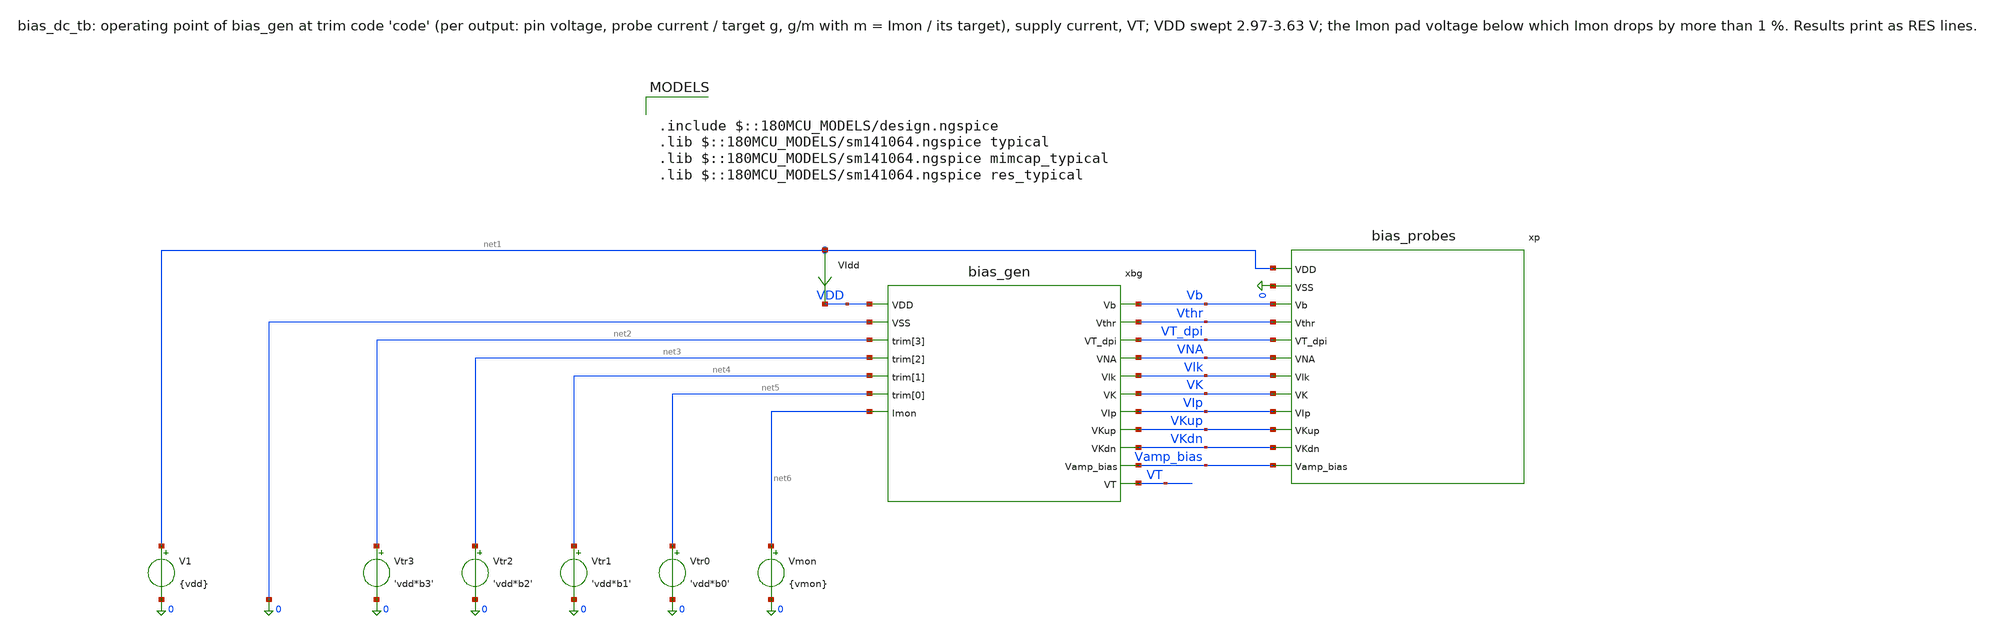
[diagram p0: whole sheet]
** sch_path: analog/bias/testbenches/bias_dc_tb.sch
**.subckt bias_dc_tb
xbg VDD 0 net2 net3 net4 net5 net6 Vb Vthr VT_dpi VNA Vlk VK VIp VKup VKdn Vamp_bias VT bias_gen
V1 net1 0 {vdd}
VIdd net1 VDD 0
.save i(vidd)
Vtr3 net2 0 'vdd*b3'
Vtr2 net3 0 'vdd*b2'
Vtr1 net4 0 'vdd*b1'
Vtr0 net5 0 'vdd*b0'
Vmon net6 0 {vmon}
xp net1 0 Vb Vthr VT_dpi VNA Vlk VK VIp VKup VKdn Vamp_bias bias_probes
**** begin user architecture code

.include $::180MCU_MODELS/design.ngspice
.lib $::180MCU_MODELS/sm141064.ngspice typical
.lib $::180MCU_MODELS/sm141064.ngspice mimcap_typical
.lib $::180MCU_MODELS/sm141064.ngspice res_typical



* Reference: tt, 27 C, trim code 9 (see analog/testbenches/README.md)
.param vdd=3.3 code=9 vmon=1.65
* trim bits of 'code' (b3 = MSB), driven by Vtr3..Vtr0
.param b3='floor(code/8)-2*floor(code/16)' b2='floor(code/4)-2*floor(code/8)'
.param b1='floor(code/2)-2*floor(code/4)' b0='code-2*floor(code/2)'
.csparam code_c={code}
.csparam vdd_c={vdd}
.control
  save all
  op
  let tr = 1/(0.743 + (15 - code_c)*0.045133)
  let m = abs(i(Vmon))/(2.3072e-07*tr)
  let g_Vb = abs(i(v.xp.vp_vb))/1.442e-08
  let g_Vthr = abs(i(v.xp.vp_vthr))/7.367e-11
  let g_VT_dpi = abs(i(v.xp.vp_vt_dpi))/9.37e-11
  let g_VNA = abs(i(v.xp.vp_vna))/5.049e-06
  let g_Vlk = abs(i(v.xp.vp_vlk))/5.415e-10
  let g_VK = abs(i(v.xp.vp_vk))/1.752e-05
  let g_VIp = abs(i(v.xp.vp_vip))/2.402e-08
  let g_VKup = abs(i(v.xp.vp_vkup))/5.513e-07
  let g_VKdn = abs(i(v.xp.vp_vkdn))/3.418e-08
  let g_Vamp_bias = abs(i(v.xp.vp_vamp_bias))/9.654e-08
  let itot = abs(i(VIdd))
  echo RES m=$&m
  echo RES itot=$&itot
  echo RES vt=$&v(VT)
  echo RES v_Vb=$&v(Vb)
  let gm_Vb = g_Vb/m
  echo RES gm_Vb=$&gm_Vb
  set gm0_Vb = $&gm_Vb
  echo RES v_Vthr=$&v(Vthr)
  let gm_Vthr = g_Vthr/m
  echo RES gm_Vthr=$&gm_Vthr
  set gm0_Vthr = $&gm_Vthr
  echo RES v_VT_dpi=$&v(VT_dpi)
  let gm_VT_dpi = g_VT_dpi/m
  echo RES gm_VT_dpi=$&gm_VT_dpi
  set gm0_VT_dpi = $&gm_VT_dpi
  echo RES v_VNA=$&v(VNA)
  let gm_VNA = g_VNA/m
  echo RES gm_VNA=$&gm_VNA
  set gm0_VNA = $&gm_VNA
  echo RES v_Vlk=$&v(Vlk)
  let gm_Vlk = g_Vlk/m
  echo RES gm_Vlk=$&gm_Vlk
  set gm0_Vlk = $&gm_Vlk
  echo RES v_VK=$&v(VK)
  let gm_VK = g_VK/m
  echo RES gm_VK=$&gm_VK
  set gm0_VK = $&gm_VK
  echo RES v_VIp=$&v(VIp)
  let gm_VIp = g_VIp/m
  echo RES gm_VIp=$&gm_VIp
  set gm0_VIp = $&gm_VIp
  echo RES v_VKup=$&v(VKup)
  let gm_VKup = g_VKup/m
  echo RES gm_VKup=$&gm_VKup
  set gm0_VKup = $&gm_VKup
  echo RES v_VKdn=$&v(VKdn)
  let gm_VKdn = g_VKdn/m
  echo RES gm_VKdn=$&gm_VKdn
  set gm0_VKdn = $&gm_VKdn
  echo RES v_Vamp_bias=$&v(Vamp_bias)
  let gm_Vamp_bias = g_Vamp_bias/m
  echo RES gm_Vamp_bias=$&gm_Vamp_bias
  set gm0_Vamp_bias = $&gm_Vamp_bias

  * supply 2.97-3.63 V (+-10 %): worst |(g/m)(VDD) / (g/m)(3.3 V) - 1| per output
  dc V1 2.97 3.63 0.11
  let tr = 1/(0.743 + (15 - code_c)*0.045133)
  let m = abs(i(Vmon))/(2.3072e-07*tr)
  let g_Vb = abs(i(v.xp.vp_vb))/1.442e-08
  let g_Vthr = abs(i(v.xp.vp_vthr))/7.367e-11
  let g_VT_dpi = abs(i(v.xp.vp_vt_dpi))/9.37e-11
  let g_VNA = abs(i(v.xp.vp_vna))/5.049e-06
  let g_Vlk = abs(i(v.xp.vp_vlk))/5.415e-10
  let g_VK = abs(i(v.xp.vp_vk))/1.752e-05
  let g_VIp = abs(i(v.xp.vp_vip))/2.402e-08
  let g_VKup = abs(i(v.xp.vp_vkup))/5.513e-07
  let g_VKdn = abs(i(v.xp.vp_vkdn))/3.418e-08
  let g_Vamp_bias = abs(i(v.xp.vp_vamp_bias))/9.654e-08
  let e_Vb = abs(g_Vb/m/$gm0_Vb - 1)
  meas dc ev_Vb max e_Vb
  echo RES ev_Vb=$&ev_Vb
  let e_Vthr = abs(g_Vthr/m/$gm0_Vthr - 1)
  meas dc ev_Vthr max e_Vthr
  echo RES ev_Vthr=$&ev_Vthr
  let e_VT_dpi = abs(g_VT_dpi/m/$gm0_VT_dpi - 1)
  meas dc ev_VT_dpi max e_VT_dpi
  echo RES ev_VT_dpi=$&ev_VT_dpi
  let e_VNA = abs(g_VNA/m/$gm0_VNA - 1)
  meas dc ev_VNA max e_VNA
  echo RES ev_VNA=$&ev_VNA
  let e_Vlk = abs(g_Vlk/m/$gm0_Vlk - 1)
  meas dc ev_Vlk max e_Vlk
  echo RES ev_Vlk=$&ev_Vlk
  let e_VK = abs(g_VK/m/$gm0_VK - 1)
  meas dc ev_VK max e_VK
  echo RES ev_VK=$&ev_VK
  let e_VIp = abs(g_VIp/m/$gm0_VIp - 1)
  meas dc ev_VIp max e_VIp
  echo RES ev_VIp=$&ev_VIp
  let e_VKup = abs(g_VKup/m/$gm0_VKup - 1)
  meas dc ev_VKup max e_VKup
  echo RES ev_VKup=$&ev_VKup
  let e_VKdn = abs(g_VKdn/m/$gm0_VKdn - 1)
  meas dc ev_VKdn max e_VKdn
  echo RES ev_VKdn=$&ev_VKdn
  let e_Vamp_bias = abs(g_Vamp_bias/m/$gm0_Vamp_bias - 1)
  meas dc ev_Vamp_bias max e_Vamp_bias
  echo RES ev_Vamp_bias=$&ev_Vamp_bias

  * Imon pad: lowest pad voltage with Imon within 1 % of its 1.65 V value
  dc Vmon 0 3.3 0.01
  let imon = abs(i(Vmon))
  meas dc i165 find imon at=1.65
  let r = imon/i165
  meas dc imon_vmin when r=0.99 cross=1
  echo RES imon_vmin=$&imon_vmin
  if $?batchmode = 0
    plot r title 'Imon / Imon(1.65 V) vs pad voltage'
  end
.endc


**** end user architecture code
**.ends

* expanding   symbol:  analog/bias/bias_gen.sym # of pins=18
** sym_path: analog/bias/bias_gen.sym
** sch_path: analog/bias/bias_gen.sch
.subckt bias_gen VDD VSS trim[3] trim[2] trim[1] trim[0] Imon Vb Vthr VT_dpi VNA Vlk VK VIp VKup
+ VKdn Vamp_bias VT
*.iopin VDD
*.iopin VSS
*.ipin trim[3]
*.ipin trim[2]
*.ipin trim[1]
*.ipin trim[0]
*.iopin Imon
*.opin Vb
*.opin Vthr
*.opin VT_dpi
*.opin VNA
*.opin Vlk
*.opin VK
*.opin VIp
*.opin VKup
*.opin VKdn
*.opin Vamp_bias
*.opin VT
XM3 Vgp Vgp VDD VDD pfet_03v3 L=6.0u W=1.0u nf=1 ad='int((nf+1)/2) * W/nf * 0.18u' as='int((nf+2)/2) * W/nf * 0.18u'
+ pd='2*int((nf+1)/2) * (W/nf + 0.18u)' ps='2*int((nf+2)/2) * (W/nf + 0.18u)' nrd='0.18u / W' nrs='0.18u / W'
+ sa=0 sb=0 sd=0 m=4
XM4 Vgn Vgp VDD VDD pfet_03v3 L=6.0u W=1.0u nf=1 ad='int((nf+1)/2) * W/nf * 0.18u' as='int((nf+2)/2) * W/nf * 0.18u'
+ pd='2*int((nf+1)/2) * (W/nf + 0.18u)' ps='2*int((nf+2)/2) * (W/nf + 0.18u)' nrd='0.18u / W' nrs='0.18u / W'
+ sa=0 sb=0 sd=0 m=4
XM2 Vgp Vgn Vr VSS nfet_03v3 L=6.0u W=1.0u nf=1 ad='int((nf+1)/2) * W/nf * 0.18u' as='int((nf+2)/2) * W/nf * 0.18u'
+ pd='2*int((nf+1)/2) * (W/nf + 0.18u)' ps='2*int((nf+2)/2) * (W/nf + 0.18u)' nrd='0.18u / W' nrs='0.18u / W'
+ sa=0 sb=0 sd=0 m=64
XM1 Vgn Vgn VSS VSS nfet_03v3 L=6.0u W=1.0u nf=1 ad='int((nf+1)/2) * W/nf * 0.18u' as='int((nf+2)/2) * W/nf * 0.18u'
+ pd='2*int((nf+1)/2) * (W/nf + 0.18u)' ps='2*int((nf+2)/2) * (W/nf + 0.18u)' nrd='0.18u / W' nrs='0.18u / W'
+ sa=0 sb=0 sd=0 m=8
XR15 t3 Vr VSS nwell r_width=2.0e-6 r_length=367.830e-6 m=1
XRT3 t2 t3 VSS nwell r_width=2.0e-6 r_length=178.750e-6 m=1
XMT3 t3 trim[3] t2 VSS nfet_03v3 L=0.28u W=4.0u nf=1 ad='int((nf+1)/2) * W/nf * 0.18u' as='int((nf+2)/2) * W/nf * 0.18u'
+ pd='2*int((nf+1)/2) * (W/nf + 0.18u)' ps='2*int((nf+2)/2) * (W/nf + 0.18u)' nrd='0.18u / W' nrs='0.18u / W'
+ sa=0 sb=0 sd=0 m=4
XRT2 t1 t2 VSS nwell r_width=2.0e-6 r_length=89.375e-6 m=1
XMT2 t2 trim[2] t1 VSS nfet_03v3 L=0.28u W=4.0u nf=1 ad='int((nf+1)/2) * W/nf * 0.18u' as='int((nf+2)/2) * W/nf * 0.18u'
+ pd='2*int((nf+1)/2) * (W/nf + 0.18u)' ps='2*int((nf+2)/2) * (W/nf + 0.18u)' nrd='0.18u / W' nrs='0.18u / W'
+ sa=0 sb=0 sd=0 m=2
XRT1 t0 t1 VSS nwell r_width=2.0e-6 r_length=44.687e-6 m=1
XMT1 t1 trim[1] t0 VSS nfet_03v3 L=0.28u W=4.0u nf=1 ad='int((nf+1)/2) * W/nf * 0.18u' as='int((nf+2)/2) * W/nf * 0.18u'
+ pd='2*int((nf+1)/2) * (W/nf + 0.18u)' ps='2*int((nf+2)/2) * (W/nf + 0.18u)' nrd='0.18u / W' nrs='0.18u / W'
+ sa=0 sb=0 sd=0 m=1
XRT0 VSS t0 VSS nwell r_width=2.0e-6 r_length=22.344e-6 m=1
XMT0 t0 trim[0] VSS VSS nfet_03v3 L=0.28u W=4.0u nf=1 ad='int((nf+1)/2) * W/nf * 0.18u' as='int((nf+2)/2) * W/nf * 0.18u'
+ pd='2*int((nf+1)/2) * (W/nf + 0.18u)' ps='2*int((nf+2)/2) * (W/nf + 0.18u)' nrd='0.18u / W' nrs='0.18u / W'
+ sa=0 sb=0 sd=0 m=1
XMS1_0 net1 VSS VDD VDD pfet_03v3 L=50u W=0.22u nf=1 ad='int((nf+1)/2) * W/nf * 0.18u' as='int((nf+2)/2) * W/nf * 0.18u'
+ pd='2*int((nf+1)/2) * (W/nf + 0.18u)' ps='2*int((nf+2)/2) * (W/nf + 0.18u)' nrd='0.18u / W' nrs='0.18u / W'
+ sa=0 sb=0 sd=0 m=1
XMS1_1 net2 VSS net1 VDD pfet_03v3 L=50u W=0.22u nf=1 ad='int((nf+1)/2) * W/nf * 0.18u' as='int((nf+2)/2) * W/nf * 0.18u'
+ pd='2*int((nf+1)/2) * (W/nf + 0.18u)' ps='2*int((nf+2)/2) * (W/nf + 0.18u)' nrd='0.18u / W' nrs='0.18u / W'
+ sa=0 sb=0 sd=0 m=1
XMS1_2 net3 VSS net2 VDD pfet_03v3 L=50u W=0.22u nf=1 ad='int((nf+1)/2) * W/nf * 0.18u' as='int((nf+2)/2) * W/nf * 0.18u'
+ pd='2*int((nf+1)/2) * (W/nf + 0.18u)' ps='2*int((nf+2)/2) * (W/nf + 0.18u)' nrd='0.18u / W' nrs='0.18u / W'
+ sa=0 sb=0 sd=0 m=1
XMS1_3 X VSS net3 VDD pfet_03v3 L=50u W=0.22u nf=1 ad='int((nf+1)/2) * W/nf * 0.18u' as='int((nf+2)/2) * W/nf * 0.18u'
+ pd='2*int((nf+1)/2) * (W/nf + 0.18u)' ps='2*int((nf+2)/2) * (W/nf + 0.18u)' nrd='0.18u / W' nrs='0.18u / W'
+ sa=0 sb=0 sd=0 m=1
XMS2 X Vgn VSS VSS nfet_03v3 L=6.0u W=1.0u nf=1 ad='int((nf+1)/2) * W/nf * 0.18u' as='int((nf+2)/2) * W/nf * 0.18u'
+ pd='2*int((nf+1)/2) * (W/nf + 0.18u)' ps='2*int((nf+2)/2) * (W/nf + 0.18u)' nrd='0.18u / W' nrs='0.18u / W'
+ sa=0 sb=0 sd=0 m=16
XMS3 Vgp X VSS VSS nfet_03v3 L=4u W=0.5u nf=1 ad='int((nf+1)/2) * W/nf * 0.18u' as='int((nf+2)/2) * W/nf * 0.18u'
+ pd='2*int((nf+1)/2) * (W/nf + 0.18u)' ps='2*int((nf+2)/2) * (W/nf + 0.18u)' nrd='0.18u / W' nrs='0.18u / W'
+ sa=0 sb=0 sd=0 m=1
XMMON Imon Vgn VSS VSS nfet_03v3 L=6.0u W=1.0u nf=1 ad='int((nf+1)/2) * W/nf * 0.18u' as='int((nf+2)/2) * W/nf * 0.18u'
+ pd='2*int((nf+1)/2) * (W/nf + 0.18u)' ps='2*int((nf+2)/2) * (W/nf + 0.18u)' nrd='0.18u / W' nrs='0.18u / W'
+ sa=0 sb=0 sd=0 m=8
XMOVB_0 net4 Vgp VDD VDD pfet_03v3 L=6.0u W=1.0u nf=1 ad='int((nf+1)/2) * W/nf * 0.18u' as='int((nf+2)/2) * W/nf * 0.18u'
+ pd='2*int((nf+1)/2) * (W/nf + 0.18u)' ps='2*int((nf+2)/2) * (W/nf + 0.18u)' nrd='0.18u / W' nrs='0.18u / W'
+ sa=0 sb=0 sd=0 m=5
XMOVB_1 net5 Vgp net4 VDD pfet_03v3 L=6.0u W=1.0u nf=1 ad='int((nf+1)/2) * W/nf * 0.18u' as='int((nf+2)/2) * W/nf * 0.18u'
+ pd='2*int((nf+1)/2) * (W/nf + 0.18u)' ps='2*int((nf+2)/2) * (W/nf + 0.18u)' nrd='0.18u / W' nrs='0.18u / W'
+ sa=0 sb=0 sd=0 m=5
XMOVB_2 net6 Vgp net5 VDD pfet_03v3 L=6.0u W=1.0u nf=1 ad='int((nf+1)/2) * W/nf * 0.18u' as='int((nf+2)/2) * W/nf * 0.18u'
+ pd='2*int((nf+1)/2) * (W/nf + 0.18u)' ps='2*int((nf+2)/2) * (W/nf + 0.18u)' nrd='0.18u / W' nrs='0.18u / W'
+ sa=0 sb=0 sd=0 m=5
XMOVB_3 net7 Vgp net6 VDD pfet_03v3 L=6.0u W=1.0u nf=1 ad='int((nf+1)/2) * W/nf * 0.18u' as='int((nf+2)/2) * W/nf * 0.18u'
+ pd='2*int((nf+1)/2) * (W/nf + 0.18u)' ps='2*int((nf+2)/2) * (W/nf + 0.18u)' nrd='0.18u / W' nrs='0.18u / W'
+ sa=0 sb=0 sd=0 m=5
XMOVB_4 net8 Vgp net7 VDD pfet_03v3 L=6.0u W=1.0u nf=1 ad='int((nf+1)/2) * W/nf * 0.18u' as='int((nf+2)/2) * W/nf * 0.18u'
+ pd='2*int((nf+1)/2) * (W/nf + 0.18u)' ps='2*int((nf+2)/2) * (W/nf + 0.18u)' nrd='0.18u / W' nrs='0.18u / W'
+ sa=0 sb=0 sd=0 m=5
XMOVB_5 Vb Vgp net8 VDD pfet_03v3 L=6.0u W=1.0u nf=1 ad='int((nf+1)/2) * W/nf * 0.18u' as='int((nf+2)/2) * W/nf * 0.18u'
+ pd='2*int((nf+1)/2) * (W/nf + 0.18u)' ps='2*int((nf+2)/2) * (W/nf + 0.18u)' nrd='0.18u / W' nrs='0.18u / W'
+ sa=0 sb=0 sd=0 m=5
XMRVB Vb Vb VSS VSS nfet_03v3 L=8.0u W=1.0u nf=1 ad='int((nf+1)/2) * W/nf * 0.18u' as='int((nf+2)/2) * W/nf * 0.18u'
+ pd='2*int((nf+1)/2) * (W/nf + 0.18u)' ps='2*int((nf+2)/2) * (W/nf + 0.18u)' nrd='0.18u / W' nrs='0.18u / W'
+ sa=0 sb=0 sd=0 m=3
XMCVB VSS Vb VSS VSS nfet_03v3 L=10.0u W=10.0u nf=1 ad='int((nf+1)/2) * W/nf * 0.18u' as='int((nf+2)/2) * W/nf * 0.18u'
+ pd='2*int((nf+1)/2) * (W/nf + 0.18u)' ps='2*int((nf+2)/2) * (W/nf + 0.18u)' nrd='0.18u / W' nrs='0.18u / W'
+ sa=0 sb=0 sd=0 m=1
XMRVTHR Vthr Vthr VDD VDD pfet_03v3 L=0.28u W=0.22u nf=1 ad='int((nf+1)/2) * W/nf * 0.18u' as='int((nf+2)/2) * W/nf * 0.18u'
+ pd='2*int((nf+1)/2) * (W/nf + 0.18u)' ps='2*int((nf+2)/2) * (W/nf + 0.18u)' nrd='0.18u / W' nrs='0.18u / W'
+ sa=0 sb=0 sd=0 m=32
XMOVTHR_0 Vthr Vgn net9 VSS nfet_03v3 L=6.0u W=1.0u nf=1 ad='int((nf+1)/2) * W/nf * 0.18u' as='int((nf+2)/2) * W/nf * 0.18u'
+ pd='2*int((nf+1)/2) * (W/nf + 0.18u)' ps='2*int((nf+2)/2) * (W/nf + 0.18u)' nrd='0.18u / W' nrs='0.18u / W'
+ sa=0 sb=0 sd=0 m=1
XMOVTHR_1 net9 Vgn net10 VSS nfet_03v3 L=6.0u W=1.0u nf=1 ad='int((nf+1)/2) * W/nf * 0.18u' as='int((nf+2)/2) * W/nf * 0.18u'
+ pd='2*int((nf+1)/2) * (W/nf + 0.18u)' ps='2*int((nf+2)/2) * (W/nf + 0.18u)' nrd='0.18u / W' nrs='0.18u / W'
+ sa=0 sb=0 sd=0 m=1
XMOVTHR_2 net10 Vgn net11 VSS nfet_03v3 L=6.0u W=1.0u nf=1 ad='int((nf+1)/2) * W/nf * 0.18u' as='int((nf+2)/2) * W/nf * 0.18u'
+ pd='2*int((nf+1)/2) * (W/nf + 0.18u)' ps='2*int((nf+2)/2) * (W/nf + 0.18u)' nrd='0.18u / W' nrs='0.18u / W'
+ sa=0 sb=0 sd=0 m=1
XMOVTHR_3 net11 Vgn net12 VSS nfet_03v3 L=6.0u W=1.0u nf=1 ad='int((nf+1)/2) * W/nf * 0.18u' as='int((nf+2)/2) * W/nf * 0.18u'
+ pd='2*int((nf+1)/2) * (W/nf + 0.18u)' ps='2*int((nf+2)/2) * (W/nf + 0.18u)' nrd='0.18u / W' nrs='0.18u / W'
+ sa=0 sb=0 sd=0 m=1
XMOVTHR_4 net12 Vgn net13 VSS nfet_03v3 L=6.0u W=1.0u nf=1 ad='int((nf+1)/2) * W/nf * 0.18u' as='int((nf+2)/2) * W/nf * 0.18u'
+ pd='2*int((nf+1)/2) * (W/nf + 0.18u)' ps='2*int((nf+2)/2) * (W/nf + 0.18u)' nrd='0.18u / W' nrs='0.18u / W'
+ sa=0 sb=0 sd=0 m=1
XMOVTHR_5 net13 Vgn net14 VSS nfet_03v3 L=6.0u W=1.0u nf=1 ad='int((nf+1)/2) * W/nf * 0.18u' as='int((nf+2)/2) * W/nf * 0.18u'
+ pd='2*int((nf+1)/2) * (W/nf + 0.18u)' ps='2*int((nf+2)/2) * (W/nf + 0.18u)' nrd='0.18u / W' nrs='0.18u / W'
+ sa=0 sb=0 sd=0 m=1
XMOVTHR_6 net14 Vgn net15 VSS nfet_03v3 L=6.0u W=1.0u nf=1 ad='int((nf+1)/2) * W/nf * 0.18u' as='int((nf+2)/2) * W/nf * 0.18u'
+ pd='2*int((nf+1)/2) * (W/nf + 0.18u)' ps='2*int((nf+2)/2) * (W/nf + 0.18u)' nrd='0.18u / W' nrs='0.18u / W'
+ sa=0 sb=0 sd=0 m=1
XMOVTHR_7 net15 Vgn net16 VSS nfet_03v3 L=6.0u W=1.0u nf=1 ad='int((nf+1)/2) * W/nf * 0.18u' as='int((nf+2)/2) * W/nf * 0.18u'
+ pd='2*int((nf+1)/2) * (W/nf + 0.18u)' ps='2*int((nf+2)/2) * (W/nf + 0.18u)' nrd='0.18u / W' nrs='0.18u / W'
+ sa=0 sb=0 sd=0 m=1
XMOVTHR_8 net16 Vgn net17 VSS nfet_03v3 L=6.0u W=1.0u nf=1 ad='int((nf+1)/2) * W/nf * 0.18u' as='int((nf+2)/2) * W/nf * 0.18u'
+ pd='2*int((nf+1)/2) * (W/nf + 0.18u)' ps='2*int((nf+2)/2) * (W/nf + 0.18u)' nrd='0.18u / W' nrs='0.18u / W'
+ sa=0 sb=0 sd=0 m=1
XMOVTHR_9 net17 Vgn net18 VSS nfet_03v3 L=6.0u W=1.0u nf=1 ad='int((nf+1)/2) * W/nf * 0.18u' as='int((nf+2)/2) * W/nf * 0.18u'
+ pd='2*int((nf+1)/2) * (W/nf + 0.18u)' ps='2*int((nf+2)/2) * (W/nf + 0.18u)' nrd='0.18u / W' nrs='0.18u / W'
+ sa=0 sb=0 sd=0 m=1
XMOVTHR_10 net18 Vgn net19 VSS nfet_03v3 L=6.0u W=1.0u nf=1 ad='int((nf+1)/2) * W/nf * 0.18u' as='int((nf+2)/2) * W/nf * 0.18u'
+ pd='2*int((nf+1)/2) * (W/nf + 0.18u)' ps='2*int((nf+2)/2) * (W/nf + 0.18u)' nrd='0.18u / W' nrs='0.18u / W'
+ sa=0 sb=0 sd=0 m=1
XMOVTHR_11 net19 Vgn net20 VSS nfet_03v3 L=6.0u W=1.0u nf=1 ad='int((nf+1)/2) * W/nf * 0.18u' as='int((nf+2)/2) * W/nf * 0.18u'
+ pd='2*int((nf+1)/2) * (W/nf + 0.18u)' ps='2*int((nf+2)/2) * (W/nf + 0.18u)' nrd='0.18u / W' nrs='0.18u / W'
+ sa=0 sb=0 sd=0 m=1
XMOVTHR_12 net20 Vgn net21 VSS nfet_03v3 L=6.0u W=1.0u nf=1 ad='int((nf+1)/2) * W/nf * 0.18u' as='int((nf+2)/2) * W/nf * 0.18u'
+ pd='2*int((nf+1)/2) * (W/nf + 0.18u)' ps='2*int((nf+2)/2) * (W/nf + 0.18u)' nrd='0.18u / W' nrs='0.18u / W'
+ sa=0 sb=0 sd=0 m=1
XMOVTHR_13 net21 Vgn net22 VSS nfet_03v3 L=6.0u W=1.0u nf=1 ad='int((nf+1)/2) * W/nf * 0.18u' as='int((nf+2)/2) * W/nf * 0.18u'
+ pd='2*int((nf+1)/2) * (W/nf + 0.18u)' ps='2*int((nf+2)/2) * (W/nf + 0.18u)' nrd='0.18u / W' nrs='0.18u / W'
+ sa=0 sb=0 sd=0 m=1
XMOVTHR_14 net22 Vgn VSS VSS nfet_03v3 L=6.0u W=1.0u nf=1 ad='int((nf+1)/2) * W/nf * 0.18u' as='int((nf+2)/2) * W/nf * 0.18u'
+ pd='2*int((nf+1)/2) * (W/nf + 0.18u)' ps='2*int((nf+2)/2) * (W/nf + 0.18u)' nrd='0.18u / W' nrs='0.18u / W'
+ sa=0 sb=0 sd=0 m=1
XMCVTHR VDD Vthr VDD VDD pfet_03v3 L=10.0u W=10.0u nf=1 ad='int((nf+1)/2) * W/nf * 0.18u' as='int((nf+2)/2) * W/nf * 0.18u'
+ pd='2*int((nf+1)/2) * (W/nf + 0.18u)' ps='2*int((nf+2)/2) * (W/nf + 0.18u)' nrd='0.18u / W' nrs='0.18u / W'
+ sa=0 sb=0 sd=0 m=1
XMRVT_DPI VT_dpi VT_dpi VDD VDD pfet_03v3 L=0.28u W=0.22u nf=1 ad='int((nf+1)/2) * W/nf * 0.18u' as='int((nf+2)/2) * W/nf * 0.18u'
+ pd='2*int((nf+1)/2) * (W/nf + 0.18u)' ps='2*int((nf+2)/2) * (W/nf + 0.18u)' nrd='0.18u / W' nrs='0.18u / W'
+ sa=0 sb=0 sd=0 m=32
XMOVT_DPI_0 VT_dpi Vgn net23 VSS nfet_03v3 L=6.0u W=1.0u nf=1 ad='int((nf+1)/2) * W/nf * 0.18u' as='int((nf+2)/2) * W/nf * 0.18u'
+ pd='2*int((nf+1)/2) * (W/nf + 0.18u)' ps='2*int((nf+2)/2) * (W/nf + 0.18u)' nrd='0.18u / W' nrs='0.18u / W'
+ sa=0 sb=0 sd=0 m=2
XMOVT_DPI_1 net23 Vgn net24 VSS nfet_03v3 L=6.0u W=1.0u nf=1 ad='int((nf+1)/2) * W/nf * 0.18u' as='int((nf+2)/2) * W/nf * 0.18u'
+ pd='2*int((nf+1)/2) * (W/nf + 0.18u)' ps='2*int((nf+2)/2) * (W/nf + 0.18u)' nrd='0.18u / W' nrs='0.18u / W'
+ sa=0 sb=0 sd=0 m=2
XMOVT_DPI_2 net24 Vgn net25 VSS nfet_03v3 L=6.0u W=1.0u nf=1 ad='int((nf+1)/2) * W/nf * 0.18u' as='int((nf+2)/2) * W/nf * 0.18u'
+ pd='2*int((nf+1)/2) * (W/nf + 0.18u)' ps='2*int((nf+2)/2) * (W/nf + 0.18u)' nrd='0.18u / W' nrs='0.18u / W'
+ sa=0 sb=0 sd=0 m=2
XMOVT_DPI_3 net25 Vgn net26 VSS nfet_03v3 L=6.0u W=1.0u nf=1 ad='int((nf+1)/2) * W/nf * 0.18u' as='int((nf+2)/2) * W/nf * 0.18u'
+ pd='2*int((nf+1)/2) * (W/nf + 0.18u)' ps='2*int((nf+2)/2) * (W/nf + 0.18u)' nrd='0.18u / W' nrs='0.18u / W'
+ sa=0 sb=0 sd=0 m=2
XMOVT_DPI_4 net26 Vgn net27 VSS nfet_03v3 L=6.0u W=1.0u nf=1 ad='int((nf+1)/2) * W/nf * 0.18u' as='int((nf+2)/2) * W/nf * 0.18u'
+ pd='2*int((nf+1)/2) * (W/nf + 0.18u)' ps='2*int((nf+2)/2) * (W/nf + 0.18u)' nrd='0.18u / W' nrs='0.18u / W'
+ sa=0 sb=0 sd=0 m=2
XMOVT_DPI_5 net27 Vgn net28 VSS nfet_03v3 L=6.0u W=1.0u nf=1 ad='int((nf+1)/2) * W/nf * 0.18u' as='int((nf+2)/2) * W/nf * 0.18u'
+ pd='2*int((nf+1)/2) * (W/nf + 0.18u)' ps='2*int((nf+2)/2) * (W/nf + 0.18u)' nrd='0.18u / W' nrs='0.18u / W'
+ sa=0 sb=0 sd=0 m=2
XMOVT_DPI_6 net28 Vgn net29 VSS nfet_03v3 L=6.0u W=1.0u nf=1 ad='int((nf+1)/2) * W/nf * 0.18u' as='int((nf+2)/2) * W/nf * 0.18u'
+ pd='2*int((nf+1)/2) * (W/nf + 0.18u)' ps='2*int((nf+2)/2) * (W/nf + 0.18u)' nrd='0.18u / W' nrs='0.18u / W'
+ sa=0 sb=0 sd=0 m=2
XMOVT_DPI_7 net29 Vgn net30 VSS nfet_03v3 L=6.0u W=1.0u nf=1 ad='int((nf+1)/2) * W/nf * 0.18u' as='int((nf+2)/2) * W/nf * 0.18u'
+ pd='2*int((nf+1)/2) * (W/nf + 0.18u)' ps='2*int((nf+2)/2) * (W/nf + 0.18u)' nrd='0.18u / W' nrs='0.18u / W'
+ sa=0 sb=0 sd=0 m=2
XMOVT_DPI_8 net30 Vgn net31 VSS nfet_03v3 L=6.0u W=1.0u nf=1 ad='int((nf+1)/2) * W/nf * 0.18u' as='int((nf+2)/2) * W/nf * 0.18u'
+ pd='2*int((nf+1)/2) * (W/nf + 0.18u)' ps='2*int((nf+2)/2) * (W/nf + 0.18u)' nrd='0.18u / W' nrs='0.18u / W'
+ sa=0 sb=0 sd=0 m=2
XMOVT_DPI_9 net31 Vgn net32 VSS nfet_03v3 L=6.0u W=1.0u nf=1 ad='int((nf+1)/2) * W/nf * 0.18u' as='int((nf+2)/2) * W/nf * 0.18u'
+ pd='2*int((nf+1)/2) * (W/nf + 0.18u)' ps='2*int((nf+2)/2) * (W/nf + 0.18u)' nrd='0.18u / W' nrs='0.18u / W'
+ sa=0 sb=0 sd=0 m=2
XMOVT_DPI_10 net32 Vgn net33 VSS nfet_03v3 L=6.0u W=1.0u nf=1 ad='int((nf+1)/2) * W/nf * 0.18u' as='int((nf+2)/2) * W/nf * 0.18u'
+ pd='2*int((nf+1)/2) * (W/nf + 0.18u)' ps='2*int((nf+2)/2) * (W/nf + 0.18u)' nrd='0.18u / W' nrs='0.18u / W'
+ sa=0 sb=0 sd=0 m=2
XMOVT_DPI_11 net33 Vgn net34 VSS nfet_03v3 L=6.0u W=1.0u nf=1 ad='int((nf+1)/2) * W/nf * 0.18u' as='int((nf+2)/2) * W/nf * 0.18u'
+ pd='2*int((nf+1)/2) * (W/nf + 0.18u)' ps='2*int((nf+2)/2) * (W/nf + 0.18u)' nrd='0.18u / W' nrs='0.18u / W'
+ sa=0 sb=0 sd=0 m=2
XMOVT_DPI_12 net34 Vgn net35 VSS nfet_03v3 L=6.0u W=1.0u nf=1 ad='int((nf+1)/2) * W/nf * 0.18u' as='int((nf+2)/2) * W/nf * 0.18u'
+ pd='2*int((nf+1)/2) * (W/nf + 0.18u)' ps='2*int((nf+2)/2) * (W/nf + 0.18u)' nrd='0.18u / W' nrs='0.18u / W'
+ sa=0 sb=0 sd=0 m=2
XMOVT_DPI_13 net35 Vgn net36 VSS nfet_03v3 L=6.0u W=1.0u nf=1 ad='int((nf+1)/2) * W/nf * 0.18u' as='int((nf+2)/2) * W/nf * 0.18u'
+ pd='2*int((nf+1)/2) * (W/nf + 0.18u)' ps='2*int((nf+2)/2) * (W/nf + 0.18u)' nrd='0.18u / W' nrs='0.18u / W'
+ sa=0 sb=0 sd=0 m=2
XMOVT_DPI_14 net36 Vgn net37 VSS nfet_03v3 L=6.0u W=1.0u nf=1 ad='int((nf+1)/2) * W/nf * 0.18u' as='int((nf+2)/2) * W/nf * 0.18u'
+ pd='2*int((nf+1)/2) * (W/nf + 0.18u)' ps='2*int((nf+2)/2) * (W/nf + 0.18u)' nrd='0.18u / W' nrs='0.18u / W'
+ sa=0 sb=0 sd=0 m=2
XMOVT_DPI_15 net37 Vgn net38 VSS nfet_03v3 L=6.0u W=1.0u nf=1 ad='int((nf+1)/2) * W/nf * 0.18u' as='int((nf+2)/2) * W/nf * 0.18u'
+ pd='2*int((nf+1)/2) * (W/nf + 0.18u)' ps='2*int((nf+2)/2) * (W/nf + 0.18u)' nrd='0.18u / W' nrs='0.18u / W'
+ sa=0 sb=0 sd=0 m=2
XMOVT_DPI_16 net38 Vgn net39 VSS nfet_03v3 L=6.0u W=1.0u nf=1 ad='int((nf+1)/2) * W/nf * 0.18u' as='int((nf+2)/2) * W/nf * 0.18u'
+ pd='2*int((nf+1)/2) * (W/nf + 0.18u)' ps='2*int((nf+2)/2) * (W/nf + 0.18u)' nrd='0.18u / W' nrs='0.18u / W'
+ sa=0 sb=0 sd=0 m=2
XMOVT_DPI_17 net39 Vgn net40 VSS nfet_03v3 L=6.0u W=1.0u nf=1 ad='int((nf+1)/2) * W/nf * 0.18u' as='int((nf+2)/2) * W/nf * 0.18u'
+ pd='2*int((nf+1)/2) * (W/nf + 0.18u)' ps='2*int((nf+2)/2) * (W/nf + 0.18u)' nrd='0.18u / W' nrs='0.18u / W'
+ sa=0 sb=0 sd=0 m=2
XMOVT_DPI_18 net40 Vgn net41 VSS nfet_03v3 L=6.0u W=1.0u nf=1 ad='int((nf+1)/2) * W/nf * 0.18u' as='int((nf+2)/2) * W/nf * 0.18u'
+ pd='2*int((nf+1)/2) * (W/nf + 0.18u)' ps='2*int((nf+2)/2) * (W/nf + 0.18u)' nrd='0.18u / W' nrs='0.18u / W'
+ sa=0 sb=0 sd=0 m=2
XMOVT_DPI_19 net41 Vgn net42 VSS nfet_03v3 L=6.0u W=1.0u nf=1 ad='int((nf+1)/2) * W/nf * 0.18u' as='int((nf+2)/2) * W/nf * 0.18u'
+ pd='2*int((nf+1)/2) * (W/nf + 0.18u)' ps='2*int((nf+2)/2) * (W/nf + 0.18u)' nrd='0.18u / W' nrs='0.18u / W'
+ sa=0 sb=0 sd=0 m=2
XMOVT_DPI_20 net42 Vgn net43 VSS nfet_03v3 L=6.0u W=1.0u nf=1 ad='int((nf+1)/2) * W/nf * 0.18u' as='int((nf+2)/2) * W/nf * 0.18u'
+ pd='2*int((nf+1)/2) * (W/nf + 0.18u)' ps='2*int((nf+2)/2) * (W/nf + 0.18u)' nrd='0.18u / W' nrs='0.18u / W'
+ sa=0 sb=0 sd=0 m=2
XMOVT_DPI_21 net43 Vgn net44 VSS nfet_03v3 L=6.0u W=1.0u nf=1 ad='int((nf+1)/2) * W/nf * 0.18u' as='int((nf+2)/2) * W/nf * 0.18u'
+ pd='2*int((nf+1)/2) * (W/nf + 0.18u)' ps='2*int((nf+2)/2) * (W/nf + 0.18u)' nrd='0.18u / W' nrs='0.18u / W'
+ sa=0 sb=0 sd=0 m=2
XMOVT_DPI_22 net44 Vgn VSS VSS nfet_03v3 L=6.0u W=1.0u nf=1 ad='int((nf+1)/2) * W/nf * 0.18u' as='int((nf+2)/2) * W/nf * 0.18u'
+ pd='2*int((nf+1)/2) * (W/nf + 0.18u)' ps='2*int((nf+2)/2) * (W/nf + 0.18u)' nrd='0.18u / W' nrs='0.18u / W'
+ sa=0 sb=0 sd=0 m=2
XMCVT_DPI VDD VT_dpi VDD VDD pfet_03v3 L=10.0u W=10.0u nf=1 ad='int((nf+1)/2) * W/nf * 0.18u' as='int((nf+2)/2) * W/nf * 0.18u'
+ pd='2*int((nf+1)/2) * (W/nf + 0.18u)' ps='2*int((nf+2)/2) * (W/nf + 0.18u)' nrd='0.18u / W' nrs='0.18u / W'
+ sa=0 sb=0 sd=0 m=1
XMRVNA_0 net45 VNA VDD VDD pfet_03v3 L=1.0u W=1.0u nf=1 ad='int((nf+1)/2) * W/nf * 0.18u' as='int((nf+2)/2) * W/nf * 0.18u'
+ pd='2*int((nf+1)/2) * (W/nf + 0.18u)' ps='2*int((nf+2)/2) * (W/nf + 0.18u)' nrd='0.18u / W' nrs='0.18u / W'
+ sa=0 sb=0 sd=0 m=1
XMRVNA_1 net46 VNA net45 VDD pfet_03v3 L=1.0u W=1.0u nf=1 ad='int((nf+1)/2) * W/nf * 0.18u' as='int((nf+2)/2) * W/nf * 0.18u'
+ pd='2*int((nf+1)/2) * (W/nf + 0.18u)' ps='2*int((nf+2)/2) * (W/nf + 0.18u)' nrd='0.18u / W' nrs='0.18u / W'
+ sa=0 sb=0 sd=0 m=1
XMRVNA_2 net47 VNA net46 VDD pfet_03v3 L=1.0u W=1.0u nf=1 ad='int((nf+1)/2) * W/nf * 0.18u' as='int((nf+2)/2) * W/nf * 0.18u'
+ pd='2*int((nf+1)/2) * (W/nf + 0.18u)' ps='2*int((nf+2)/2) * (W/nf + 0.18u)' nrd='0.18u / W' nrs='0.18u / W'
+ sa=0 sb=0 sd=0 m=1
XMRVNA_3 net48 VNA net47 VDD pfet_03v3 L=1.0u W=1.0u nf=1 ad='int((nf+1)/2) * W/nf * 0.18u' as='int((nf+2)/2) * W/nf * 0.18u'
+ pd='2*int((nf+1)/2) * (W/nf + 0.18u)' ps='2*int((nf+2)/2) * (W/nf + 0.18u)' nrd='0.18u / W' nrs='0.18u / W'
+ sa=0 sb=0 sd=0 m=1
XMRVNA_4 net49 VNA net48 VDD pfet_03v3 L=1.0u W=1.0u nf=1 ad='int((nf+1)/2) * W/nf * 0.18u' as='int((nf+2)/2) * W/nf * 0.18u'
+ pd='2*int((nf+1)/2) * (W/nf + 0.18u)' ps='2*int((nf+2)/2) * (W/nf + 0.18u)' nrd='0.18u / W' nrs='0.18u / W'
+ sa=0 sb=0 sd=0 m=1
XMRVNA_5 net50 VNA net49 VDD pfet_03v3 L=1.0u W=1.0u nf=1 ad='int((nf+1)/2) * W/nf * 0.18u' as='int((nf+2)/2) * W/nf * 0.18u'
+ pd='2*int((nf+1)/2) * (W/nf + 0.18u)' ps='2*int((nf+2)/2) * (W/nf + 0.18u)' nrd='0.18u / W' nrs='0.18u / W'
+ sa=0 sb=0 sd=0 m=1
XMRVNA_6 net51 VNA net50 VDD pfet_03v3 L=1.0u W=1.0u nf=1 ad='int((nf+1)/2) * W/nf * 0.18u' as='int((nf+2)/2) * W/nf * 0.18u'
+ pd='2*int((nf+1)/2) * (W/nf + 0.18u)' ps='2*int((nf+2)/2) * (W/nf + 0.18u)' nrd='0.18u / W' nrs='0.18u / W'
+ sa=0 sb=0 sd=0 m=1
XMRVNA_7 net52 VNA net51 VDD pfet_03v3 L=1.0u W=1.0u nf=1 ad='int((nf+1)/2) * W/nf * 0.18u' as='int((nf+2)/2) * W/nf * 0.18u'
+ pd='2*int((nf+1)/2) * (W/nf + 0.18u)' ps='2*int((nf+2)/2) * (W/nf + 0.18u)' nrd='0.18u / W' nrs='0.18u / W'
+ sa=0 sb=0 sd=0 m=1
XMRVNA_8 net53 VNA net52 VDD pfet_03v3 L=1.0u W=1.0u nf=1 ad='int((nf+1)/2) * W/nf * 0.18u' as='int((nf+2)/2) * W/nf * 0.18u'
+ pd='2*int((nf+1)/2) * (W/nf + 0.18u)' ps='2*int((nf+2)/2) * (W/nf + 0.18u)' nrd='0.18u / W' nrs='0.18u / W'
+ sa=0 sb=0 sd=0 m=1
XMRVNA_9 net54 VNA net53 VDD pfet_03v3 L=1.0u W=1.0u nf=1 ad='int((nf+1)/2) * W/nf * 0.18u' as='int((nf+2)/2) * W/nf * 0.18u'
+ pd='2*int((nf+1)/2) * (W/nf + 0.18u)' ps='2*int((nf+2)/2) * (W/nf + 0.18u)' nrd='0.18u / W' nrs='0.18u / W'
+ sa=0 sb=0 sd=0 m=1
XMRVNA_10 net55 VNA net54 VDD pfet_03v3 L=1.0u W=1.0u nf=1 ad='int((nf+1)/2) * W/nf * 0.18u' as='int((nf+2)/2) * W/nf * 0.18u'
+ pd='2*int((nf+1)/2) * (W/nf + 0.18u)' ps='2*int((nf+2)/2) * (W/nf + 0.18u)' nrd='0.18u / W' nrs='0.18u / W'
+ sa=0 sb=0 sd=0 m=1
XMRVNA_11 net56 VNA net55 VDD pfet_03v3 L=1.0u W=1.0u nf=1 ad='int((nf+1)/2) * W/nf * 0.18u' as='int((nf+2)/2) * W/nf * 0.18u'
+ pd='2*int((nf+1)/2) * (W/nf + 0.18u)' ps='2*int((nf+2)/2) * (W/nf + 0.18u)' nrd='0.18u / W' nrs='0.18u / W'
+ sa=0 sb=0 sd=0 m=1
XMRVNA_12 net57 VNA net56 VDD pfet_03v3 L=1.0u W=1.0u nf=1 ad='int((nf+1)/2) * W/nf * 0.18u' as='int((nf+2)/2) * W/nf * 0.18u'
+ pd='2*int((nf+1)/2) * (W/nf + 0.18u)' ps='2*int((nf+2)/2) * (W/nf + 0.18u)' nrd='0.18u / W' nrs='0.18u / W'
+ sa=0 sb=0 sd=0 m=1
XMRVNA_13 net58 VNA net57 VDD pfet_03v3 L=1.0u W=1.0u nf=1 ad='int((nf+1)/2) * W/nf * 0.18u' as='int((nf+2)/2) * W/nf * 0.18u'
+ pd='2*int((nf+1)/2) * (W/nf + 0.18u)' ps='2*int((nf+2)/2) * (W/nf + 0.18u)' nrd='0.18u / W' nrs='0.18u / W'
+ sa=0 sb=0 sd=0 m=1
XMRVNA_14 net59 VNA net58 VDD pfet_03v3 L=1.0u W=1.0u nf=1 ad='int((nf+1)/2) * W/nf * 0.18u' as='int((nf+2)/2) * W/nf * 0.18u'
+ pd='2*int((nf+1)/2) * (W/nf + 0.18u)' ps='2*int((nf+2)/2) * (W/nf + 0.18u)' nrd='0.18u / W' nrs='0.18u / W'
+ sa=0 sb=0 sd=0 m=1
XMRVNA_15 VNA VNA net59 VDD pfet_03v3 L=1.0u W=1.0u nf=1 ad='int((nf+1)/2) * W/nf * 0.18u' as='int((nf+2)/2) * W/nf * 0.18u'
+ pd='2*int((nf+1)/2) * (W/nf + 0.18u)' ps='2*int((nf+2)/2) * (W/nf + 0.18u)' nrd='0.18u / W' nrs='0.18u / W'
+ sa=0 sb=0 sd=0 m=1
XMOVNA_0 VNA Vgn net60 VSS nfet_03v3 L=6.0u W=1.0u nf=1 ad='int((nf+1)/2) * W/nf * 0.18u' as='int((nf+2)/2) * W/nf * 0.18u'
+ pd='2*int((nf+1)/2) * (W/nf + 0.18u)' ps='2*int((nf+2)/2) * (W/nf + 0.18u)' nrd='0.18u / W' nrs='0.18u / W'
+ sa=0 sb=0 sd=0 m=18
XMOVNA_1 net60 Vgn VSS VSS nfet_03v3 L=6.0u W=1.0u nf=1 ad='int((nf+1)/2) * W/nf * 0.18u' as='int((nf+2)/2) * W/nf * 0.18u'
+ pd='2*int((nf+1)/2) * (W/nf + 0.18u)' ps='2*int((nf+2)/2) * (W/nf + 0.18u)' nrd='0.18u / W' nrs='0.18u / W'
+ sa=0 sb=0 sd=0 m=18
XMCVNA VDD VNA VDD VDD pfet_03v3 L=10.0u W=10.0u nf=1 ad='int((nf+1)/2) * W/nf * 0.18u' as='int((nf+2)/2) * W/nf * 0.18u'
+ pd='2*int((nf+1)/2) * (W/nf + 0.18u)' ps='2*int((nf+2)/2) * (W/nf + 0.18u)' nrd='0.18u / W' nrs='0.18u / W'
+ sa=0 sb=0 sd=0 m=1
XMOVLK_0 net61 Vgp VDD VDD pfet_03v3 L=6.0u W=1.0u nf=1 ad='int((nf+1)/2) * W/nf * 0.18u' as='int((nf+2)/2) * W/nf * 0.18u'
+ pd='2*int((nf+1)/2) * (W/nf + 0.18u)' ps='2*int((nf+2)/2) * (W/nf + 0.18u)' nrd='0.18u / W' nrs='0.18u / W'
+ sa=0 sb=0 sd=0 m=1
XMOVLK_1 net62 Vgp net61 VDD pfet_03v3 L=6.0u W=1.0u nf=1 ad='int((nf+1)/2) * W/nf * 0.18u' as='int((nf+2)/2) * W/nf * 0.18u'
+ pd='2*int((nf+1)/2) * (W/nf + 0.18u)' ps='2*int((nf+2)/2) * (W/nf + 0.18u)' nrd='0.18u / W' nrs='0.18u / W'
+ sa=0 sb=0 sd=0 m=1
XMOVLK_2 net63 Vgp net62 VDD pfet_03v3 L=6.0u W=1.0u nf=1 ad='int((nf+1)/2) * W/nf * 0.18u' as='int((nf+2)/2) * W/nf * 0.18u'
+ pd='2*int((nf+1)/2) * (W/nf + 0.18u)' ps='2*int((nf+2)/2) * (W/nf + 0.18u)' nrd='0.18u / W' nrs='0.18u / W'
+ sa=0 sb=0 sd=0 m=1
XMOVLK_3 net64 Vgp net63 VDD pfet_03v3 L=6.0u W=1.0u nf=1 ad='int((nf+1)/2) * W/nf * 0.18u' as='int((nf+2)/2) * W/nf * 0.18u'
+ pd='2*int((nf+1)/2) * (W/nf + 0.18u)' ps='2*int((nf+2)/2) * (W/nf + 0.18u)' nrd='0.18u / W' nrs='0.18u / W'
+ sa=0 sb=0 sd=0 m=1
XMOVLK_4 net65 Vgp net64 VDD pfet_03v3 L=6.0u W=1.0u nf=1 ad='int((nf+1)/2) * W/nf * 0.18u' as='int((nf+2)/2) * W/nf * 0.18u'
+ pd='2*int((nf+1)/2) * (W/nf + 0.18u)' ps='2*int((nf+2)/2) * (W/nf + 0.18u)' nrd='0.18u / W' nrs='0.18u / W'
+ sa=0 sb=0 sd=0 m=1
XMOVLK_5 net66 Vgp net65 VDD pfet_03v3 L=6.0u W=1.0u nf=1 ad='int((nf+1)/2) * W/nf * 0.18u' as='int((nf+2)/2) * W/nf * 0.18u'
+ pd='2*int((nf+1)/2) * (W/nf + 0.18u)' ps='2*int((nf+2)/2) * (W/nf + 0.18u)' nrd='0.18u / W' nrs='0.18u / W'
+ sa=0 sb=0 sd=0 m=1
XMOVLK_6 Vlk Vgp net66 VDD pfet_03v3 L=6.0u W=1.0u nf=1 ad='int((nf+1)/2) * W/nf * 0.18u' as='int((nf+2)/2) * W/nf * 0.18u'
+ pd='2*int((nf+1)/2) * (W/nf + 0.18u)' ps='2*int((nf+2)/2) * (W/nf + 0.18u)' nrd='0.18u / W' nrs='0.18u / W'
+ sa=0 sb=0 sd=0 m=1
XMRVLK Vlk Vlk VSS VSS nfet_03v3 L=1.0u W=1.0u nf=1 ad='int((nf+1)/2) * W/nf * 0.18u' as='int((nf+2)/2) * W/nf * 0.18u'
+ pd='2*int((nf+1)/2) * (W/nf + 0.18u)' ps='2*int((nf+2)/2) * (W/nf + 0.18u)' nrd='0.18u / W' nrs='0.18u / W'
+ sa=0 sb=0 sd=0 m=14
XMCVLK VSS Vlk VSS VSS nfet_03v3 L=10.0u W=10.0u nf=1 ad='int((nf+1)/2) * W/nf * 0.18u' as='int((nf+2)/2) * W/nf * 0.18u'
+ pd='2*int((nf+1)/2) * (W/nf + 0.18u)' ps='2*int((nf+2)/2) * (W/nf + 0.18u)' nrd='0.18u / W' nrs='0.18u / W'
+ sa=0 sb=0 sd=0 m=1
XMOVK VK Vgp VDD VDD pfet_03v3 L=6.0u W=1.0u nf=1 ad='int((nf+1)/2) * W/nf * 0.18u' as='int((nf+2)/2) * W/nf * 0.18u'
+ pd='2*int((nf+1)/2) * (W/nf + 0.18u)' ps='2*int((nf+2)/2) * (W/nf + 0.18u)' nrd='0.18u / W' nrs='0.18u / W'
+ sa=0 sb=0 sd=0 m=17
XMRVK_0 VK VK net67 VSS nfet_03v3 L=1.0u W=1.0u nf=1 ad='int((nf+1)/2) * W/nf * 0.18u' as='int((nf+2)/2) * W/nf * 0.18u'
+ pd='2*int((nf+1)/2) * (W/nf + 0.18u)' ps='2*int((nf+2)/2) * (W/nf + 0.18u)' nrd='0.18u / W' nrs='0.18u / W'
+ sa=0 sb=0 sd=0 m=1
XMRVK_1 net67 VK net68 VSS nfet_03v3 L=1.0u W=1.0u nf=1 ad='int((nf+1)/2) * W/nf * 0.18u' as='int((nf+2)/2) * W/nf * 0.18u'
+ pd='2*int((nf+1)/2) * (W/nf + 0.18u)' ps='2*int((nf+2)/2) * (W/nf + 0.18u)' nrd='0.18u / W' nrs='0.18u / W'
+ sa=0 sb=0 sd=0 m=1
XMRVK_2 net68 VK net69 VSS nfet_03v3 L=1.0u W=1.0u nf=1 ad='int((nf+1)/2) * W/nf * 0.18u' as='int((nf+2)/2) * W/nf * 0.18u'
+ pd='2*int((nf+1)/2) * (W/nf + 0.18u)' ps='2*int((nf+2)/2) * (W/nf + 0.18u)' nrd='0.18u / W' nrs='0.18u / W'
+ sa=0 sb=0 sd=0 m=1
XMRVK_3 net69 VK net70 VSS nfet_03v3 L=1.0u W=1.0u nf=1 ad='int((nf+1)/2) * W/nf * 0.18u' as='int((nf+2)/2) * W/nf * 0.18u'
+ pd='2*int((nf+1)/2) * (W/nf + 0.18u)' ps='2*int((nf+2)/2) * (W/nf + 0.18u)' nrd='0.18u / W' nrs='0.18u / W'
+ sa=0 sb=0 sd=0 m=1
XMRVK_4 net70 VK net71 VSS nfet_03v3 L=1.0u W=1.0u nf=1 ad='int((nf+1)/2) * W/nf * 0.18u' as='int((nf+2)/2) * W/nf * 0.18u'
+ pd='2*int((nf+1)/2) * (W/nf + 0.18u)' ps='2*int((nf+2)/2) * (W/nf + 0.18u)' nrd='0.18u / W' nrs='0.18u / W'
+ sa=0 sb=0 sd=0 m=1
XMRVK_5 net71 VK net72 VSS nfet_03v3 L=1.0u W=1.0u nf=1 ad='int((nf+1)/2) * W/nf * 0.18u' as='int((nf+2)/2) * W/nf * 0.18u'
+ pd='2*int((nf+1)/2) * (W/nf + 0.18u)' ps='2*int((nf+2)/2) * (W/nf + 0.18u)' nrd='0.18u / W' nrs='0.18u / W'
+ sa=0 sb=0 sd=0 m=1
XMRVK_6 net72 VK net73 VSS nfet_03v3 L=1.0u W=1.0u nf=1 ad='int((nf+1)/2) * W/nf * 0.18u' as='int((nf+2)/2) * W/nf * 0.18u'
+ pd='2*int((nf+1)/2) * (W/nf + 0.18u)' ps='2*int((nf+2)/2) * (W/nf + 0.18u)' nrd='0.18u / W' nrs='0.18u / W'
+ sa=0 sb=0 sd=0 m=1
XMRVK_7 net73 VK net74 VSS nfet_03v3 L=1.0u W=1.0u nf=1 ad='int((nf+1)/2) * W/nf * 0.18u' as='int((nf+2)/2) * W/nf * 0.18u'
+ pd='2*int((nf+1)/2) * (W/nf + 0.18u)' ps='2*int((nf+2)/2) * (W/nf + 0.18u)' nrd='0.18u / W' nrs='0.18u / W'
+ sa=0 sb=0 sd=0 m=1
XMRVK_8 net74 VK net75 VSS nfet_03v3 L=1.0u W=1.0u nf=1 ad='int((nf+1)/2) * W/nf * 0.18u' as='int((nf+2)/2) * W/nf * 0.18u'
+ pd='2*int((nf+1)/2) * (W/nf + 0.18u)' ps='2*int((nf+2)/2) * (W/nf + 0.18u)' nrd='0.18u / W' nrs='0.18u / W'
+ sa=0 sb=0 sd=0 m=1
XMRVK_9 net75 VK net76 VSS nfet_03v3 L=1.0u W=1.0u nf=1 ad='int((nf+1)/2) * W/nf * 0.18u' as='int((nf+2)/2) * W/nf * 0.18u'
+ pd='2*int((nf+1)/2) * (W/nf + 0.18u)' ps='2*int((nf+2)/2) * (W/nf + 0.18u)' nrd='0.18u / W' nrs='0.18u / W'
+ sa=0 sb=0 sd=0 m=1
XMRVK_10 net76 VK net77 VSS nfet_03v3 L=1.0u W=1.0u nf=1 ad='int((nf+1)/2) * W/nf * 0.18u' as='int((nf+2)/2) * W/nf * 0.18u'
+ pd='2*int((nf+1)/2) * (W/nf + 0.18u)' ps='2*int((nf+2)/2) * (W/nf + 0.18u)' nrd='0.18u / W' nrs='0.18u / W'
+ sa=0 sb=0 sd=0 m=1
XMRVK_11 net77 VK net78 VSS nfet_03v3 L=1.0u W=1.0u nf=1 ad='int((nf+1)/2) * W/nf * 0.18u' as='int((nf+2)/2) * W/nf * 0.18u'
+ pd='2*int((nf+1)/2) * (W/nf + 0.18u)' ps='2*int((nf+2)/2) * (W/nf + 0.18u)' nrd='0.18u / W' nrs='0.18u / W'
+ sa=0 sb=0 sd=0 m=1
XMRVK_12 net78 VK net79 VSS nfet_03v3 L=1.0u W=1.0u nf=1 ad='int((nf+1)/2) * W/nf * 0.18u' as='int((nf+2)/2) * W/nf * 0.18u'
+ pd='2*int((nf+1)/2) * (W/nf + 0.18u)' ps='2*int((nf+2)/2) * (W/nf + 0.18u)' nrd='0.18u / W' nrs='0.18u / W'
+ sa=0 sb=0 sd=0 m=1
XMRVK_13 net79 VK net80 VSS nfet_03v3 L=1.0u W=1.0u nf=1 ad='int((nf+1)/2) * W/nf * 0.18u' as='int((nf+2)/2) * W/nf * 0.18u'
+ pd='2*int((nf+1)/2) * (W/nf + 0.18u)' ps='2*int((nf+2)/2) * (W/nf + 0.18u)' nrd='0.18u / W' nrs='0.18u / W'
+ sa=0 sb=0 sd=0 m=1
XMRVK_14 net80 VK net81 VSS nfet_03v3 L=1.0u W=1.0u nf=1 ad='int((nf+1)/2) * W/nf * 0.18u' as='int((nf+2)/2) * W/nf * 0.18u'
+ pd='2*int((nf+1)/2) * (W/nf + 0.18u)' ps='2*int((nf+2)/2) * (W/nf + 0.18u)' nrd='0.18u / W' nrs='0.18u / W'
+ sa=0 sb=0 sd=0 m=1
XMRVK_15 net81 VK VSS VSS nfet_03v3 L=1.0u W=1.0u nf=1 ad='int((nf+1)/2) * W/nf * 0.18u' as='int((nf+2)/2) * W/nf * 0.18u'
+ pd='2*int((nf+1)/2) * (W/nf + 0.18u)' ps='2*int((nf+2)/2) * (W/nf + 0.18u)' nrd='0.18u / W' nrs='0.18u / W'
+ sa=0 sb=0 sd=0 m=1
XMCVK VSS VK VSS VSS nfet_03v3 L=10.0u W=10.0u nf=1 ad='int((nf+1)/2) * W/nf * 0.18u' as='int((nf+2)/2) * W/nf * 0.18u'
+ pd='2*int((nf+1)/2) * (W/nf + 0.18u)' ps='2*int((nf+2)/2) * (W/nf + 0.18u)' nrd='0.18u / W' nrs='0.18u / W'
+ sa=0 sb=0 sd=0 m=1
XMOVIP VIp Vgp VDD VDD pfet_03v3 L=6.0u W=1.0u nf=1 ad='int((nf+1)/2) * W/nf * 0.18u' as='int((nf+2)/2) * W/nf * 0.18u'
+ pd='2*int((nf+1)/2) * (W/nf + 0.18u)' ps='2*int((nf+2)/2) * (W/nf + 0.18u)' nrd='0.18u / W' nrs='0.18u / W'
+ sa=0 sb=0 sd=0 m=3
XMRVIP VIp VIp VSS VSS nfet_03v3 L=1.0u W=1.0u nf=1 ad='int((nf+1)/2) * W/nf * 0.18u' as='int((nf+2)/2) * W/nf * 0.18u'
+ pd='2*int((nf+1)/2) * (W/nf + 0.18u)' ps='2*int((nf+2)/2) * (W/nf + 0.18u)' nrd='0.18u / W' nrs='0.18u / W'
+ sa=0 sb=0 sd=0 m=7
XMCVIP VSS VIp VSS VSS nfet_03v3 L=10.0u W=10.0u nf=1 ad='int((nf+1)/2) * W/nf * 0.18u' as='int((nf+2)/2) * W/nf * 0.18u'
+ pd='2*int((nf+1)/2) * (W/nf + 0.18u)' ps='2*int((nf+2)/2) * (W/nf + 0.18u)' nrd='0.18u / W' nrs='0.18u / W'
+ sa=0 sb=0 sd=0 m=1
XMRVKUP_0 net82 VKup VDD VDD pfet_03v3 L=1.0u W=1.0u nf=1 ad='int((nf+1)/2) * W/nf * 0.18u' as='int((nf+2)/2) * W/nf * 0.18u'
+ pd='2*int((nf+1)/2) * (W/nf + 0.18u)' ps='2*int((nf+2)/2) * (W/nf + 0.18u)' nrd='0.18u / W' nrs='0.18u / W'
+ sa=0 sb=0 sd=0 m=1
XMRVKUP_1 VKup VKup net82 VDD pfet_03v3 L=1.0u W=1.0u nf=1 ad='int((nf+1)/2) * W/nf * 0.18u' as='int((nf+2)/2) * W/nf * 0.18u'
+ pd='2*int((nf+1)/2) * (W/nf + 0.18u)' ps='2*int((nf+2)/2) * (W/nf + 0.18u)' nrd='0.18u / W' nrs='0.18u / W'
+ sa=0 sb=0 sd=0 m=1
XMOVKUP_0 VKup Vgn net83 VSS nfet_03v3 L=6.0u W=1.0u nf=1 ad='int((nf+1)/2) * W/nf * 0.18u' as='int((nf+2)/2) * W/nf * 0.18u'
+ pd='2*int((nf+1)/2) * (W/nf + 0.18u)' ps='2*int((nf+2)/2) * (W/nf + 0.18u)' nrd='0.18u / W' nrs='0.18u / W'
+ sa=0 sb=0 sd=0 m=16
XMOVKUP_1 net83 Vgn VSS VSS nfet_03v3 L=6.0u W=1.0u nf=1 ad='int((nf+1)/2) * W/nf * 0.18u' as='int((nf+2)/2) * W/nf * 0.18u'
+ pd='2*int((nf+1)/2) * (W/nf + 0.18u)' ps='2*int((nf+2)/2) * (W/nf + 0.18u)' nrd='0.18u / W' nrs='0.18u / W'
+ sa=0 sb=0 sd=0 m=16
XMCVKUP VDD VKup VDD VDD pfet_03v3 L=10.0u W=10.0u nf=1 ad='int((nf+1)/2) * W/nf * 0.18u' as='int((nf+2)/2) * W/nf * 0.18u'
+ pd='2*int((nf+1)/2) * (W/nf + 0.18u)' ps='2*int((nf+2)/2) * (W/nf + 0.18u)' nrd='0.18u / W' nrs='0.18u / W'
+ sa=0 sb=0 sd=0 m=1
XMOVKDN VKdn Vgp VDD VDD pfet_03v3 L=6.0u W=1.0u nf=1 ad='int((nf+1)/2) * W/nf * 0.18u' as='int((nf+2)/2) * W/nf * 0.18u'
+ pd='2*int((nf+1)/2) * (W/nf + 0.18u)' ps='2*int((nf+2)/2) * (W/nf + 0.18u)' nrd='0.18u / W' nrs='0.18u / W'
+ sa=0 sb=0 sd=0 m=5
XMRVKDN VKdn VKdn VSS VSS nfet_03v3 L=1.0u W=1.0u nf=1 ad='int((nf+1)/2) * W/nf * 0.18u' as='int((nf+2)/2) * W/nf * 0.18u'
+ pd='2*int((nf+1)/2) * (W/nf + 0.18u)' ps='2*int((nf+2)/2) * (W/nf + 0.18u)' nrd='0.18u / W' nrs='0.18u / W'
+ sa=0 sb=0 sd=0 m=8
XMCVKDN VSS VKdn VSS VSS nfet_03v3 L=10.0u W=10.0u nf=1 ad='int((nf+1)/2) * W/nf * 0.18u' as='int((nf+2)/2) * W/nf * 0.18u'
+ pd='2*int((nf+1)/2) * (W/nf + 0.18u)' ps='2*int((nf+2)/2) * (W/nf + 0.18u)' nrd='0.18u / W' nrs='0.18u / W'
+ sa=0 sb=0 sd=0 m=1
XMOVAMP_BIAS Vamp_bias Vgp VDD VDD pfet_03v3 L=6.0u W=1.0u nf=1 ad='int((nf+1)/2) * W/nf * 0.18u' as='int((nf+2)/2) * W/nf * 0.18u'
+ pd='2*int((nf+1)/2) * (W/nf + 0.18u)' ps='2*int((nf+2)/2) * (W/nf + 0.18u)' nrd='0.18u / W' nrs='0.18u / W'
+ sa=0 sb=0 sd=0 m=7
XMRVAMP_BIAS Vamp_bias Vamp_bias VSS VSS nfet_03v3 L=0.28u W=0.22u nf=1 ad='int((nf+1)/2) * W/nf * 0.18u'
+ as='int((nf+2)/2) * W/nf * 0.18u' pd='2*int((nf+1)/2) * (W/nf + 0.18u)' ps='2*int((nf+2)/2) * (W/nf + 0.18u)'
+ nrd='0.18u / W' nrs='0.18u / W' sa=0 sb=0 sd=0 m=4
XMCVAMP_BIAS VSS Vamp_bias VSS VSS nfet_03v3 L=10.0u W=10.0u nf=1 ad='int((nf+1)/2) * W/nf * 0.18u' as='int((nf+2)/2) * W/nf * 0.18u'
+ pd='2*int((nf+1)/2) * (W/nf + 0.18u)' ps='2*int((nf+2)/2) * (W/nf + 0.18u)' nrd='0.18u / W' nrs='0.18u / W'
+ sa=0 sb=0 sd=0 m=1
XMVT0 vt3 vt3 VDD VDD pfet_03v3 L=10.0u W=1.0u nf=1 ad='int((nf+1)/2) * W/nf * 0.18u' as='int((nf+2)/2) * W/nf * 0.18u'
+ pd='2*int((nf+1)/2) * (W/nf + 0.18u)' ps='2*int((nf+2)/2) * (W/nf + 0.18u)' nrd='0.18u / W' nrs='0.18u / W'
+ sa=0 sb=0 sd=0 m=1
XMVT1 VT VT vt3 vt3 pfet_03v3 L=10.0u W=1.0u nf=1 ad='int((nf+1)/2) * W/nf * 0.18u' as='int((nf+2)/2) * W/nf * 0.18u'
+ pd='2*int((nf+1)/2) * (W/nf + 0.18u)' ps='2*int((nf+2)/2) * (W/nf + 0.18u)' nrd='0.18u / W' nrs='0.18u / W'
+ sa=0 sb=0 sd=0 m=1
XMVT2 vt1 vt1 VT VT pfet_03v3 L=10.0u W=1.0u nf=1 ad='int((nf+1)/2) * W/nf * 0.18u' as='int((nf+2)/2) * W/nf * 0.18u'
+ pd='2*int((nf+1)/2) * (W/nf + 0.18u)' ps='2*int((nf+2)/2) * (W/nf + 0.18u)' nrd='0.18u / W' nrs='0.18u / W'
+ sa=0 sb=0 sd=0 m=1
XMVT3 VSS VSS vt1 vt1 pfet_03v3 L=10.0u W=1.0u nf=1 ad='int((nf+1)/2) * W/nf * 0.18u' as='int((nf+2)/2) * W/nf * 0.18u'
+ pd='2*int((nf+1)/2) * (W/nf + 0.18u)' ps='2*int((nf+2)/2) * (W/nf + 0.18u)' nrd='0.18u / W' nrs='0.18u / W'
+ sa=0 sb=0 sd=0 m=1
XMCVT VSS VT VSS VSS nfet_03v3 L=10.0u W=10.0u nf=1 ad='int((nf+1)/2) * W/nf * 0.18u' as='int((nf+2)/2) * W/nf * 0.18u'
+ pd='2*int((nf+1)/2) * (W/nf + 0.18u)' ps='2*int((nf+2)/2) * (W/nf + 0.18u)' nrd='0.18u / W' nrs='0.18u / W'
+ sa=0 sb=0 sd=0 m=1
.ends


* expanding   symbol:  analog/bias/testbenches/bias_probes.sym # of pins=12
** sym_path: analog/bias/testbenches/bias_probes.sym
** sch_path: analog/bias/testbenches/bias_probes.sch
.subckt bias_probes VDD VSS Vb Vthr VT_dpi VNA Vlk VK VIp VKup VKdn Vamp_bias
*.iopin VDD
*.iopin VSS
*.iopin Vb
*.iopin Vthr
*.iopin VT_dpi
*.iopin VNA
*.iopin Vlk
*.iopin VK
*.iopin VIp
*.iopin VKup
*.iopin VKdn
*.iopin Vamp_bias
**** begin user architecture code


* probe per bias pin: E holds the drain at the gate voltage, Vp measures the current
E_Vb pd_Vb VSS Vb VSS 1
X_Vb pd_Vb Vb ps_Vb VSS nfet_03v3 L=8.0u W=1.0u nf=1 par=1e6
Vp_Vb ps_Vb VSS 0
E_Vthr pd_Vthr VSS Vthr VSS 1
X_Vthr pd_Vthr Vthr ps_Vthr VDD pfet_03v3 L=0.28u W=0.22u nf=1 par=1e6
Vp_Vthr VDD ps_Vthr 0
E_VT_dpi pd_VT_dpi VSS VT_dpi VSS 1
X_VT_dpi pd_VT_dpi VT_dpi ps_VT_dpi VDD pfet_03v3 L=0.28u W=0.22u nf=1 par=1e6
Vp_VT_dpi VDD ps_VT_dpi 0
E_VNA pd_VNA VSS VNA VSS 1
X_VNA pd_VNA VNA ps_VNA VDD pfet_03v3 L=1.0u W=1.0u nf=1 par=1e6
Vp_VNA VDD ps_VNA 0
E_Vlk pd_Vlk VSS Vlk VSS 1
X_Vlk pd_Vlk Vlk ps_Vlk VSS nfet_03v3 L=1.0u W=1.0u nf=1 par=1e6
Vp_Vlk ps_Vlk VSS 0
E_VK pd_VK VSS VK VSS 1
X_VK pd_VK VK ps_VK VSS nfet_03v3 L=1.0u W=1.0u nf=1 par=1e6
Vp_VK ps_VK VSS 0
E_VIp pd_VIp VSS VIp VSS 1
X_VIp pd_VIp VIp ps_VIp VSS nfet_03v3 L=1.0u W=1.0u nf=1 par=1e6
Vp_VIp ps_VIp VSS 0
E_VKup pd_VKup VSS VKup VSS 1
X_VKup pd_VKup VKup ps_VKup VDD pfet_03v3 L=1.0u W=1.0u nf=1 par=1e6
Vp_VKup VDD ps_VKup 0
E_VKdn pd_VKdn VSS VKdn VSS 1
X_VKdn pd_VKdn VKdn ps_VKdn VSS nfet_03v3 L=1.0u W=1.0u nf=1 par=1e6
Vp_VKdn ps_VKdn VSS 0
E_Vamp_bias pd_Vamp_bias VSS Vamp_bias VSS 1
X_Vamp_bias pd_Vamp_bias Vamp_bias ps_Vamp_bias VSS nfet_03v3 L=0.28u W=0.22u nf=1 par=1e6
Vp_Vamp_bias ps_Vamp_bias VSS 0


**** end user architecture code
.ends

.end
